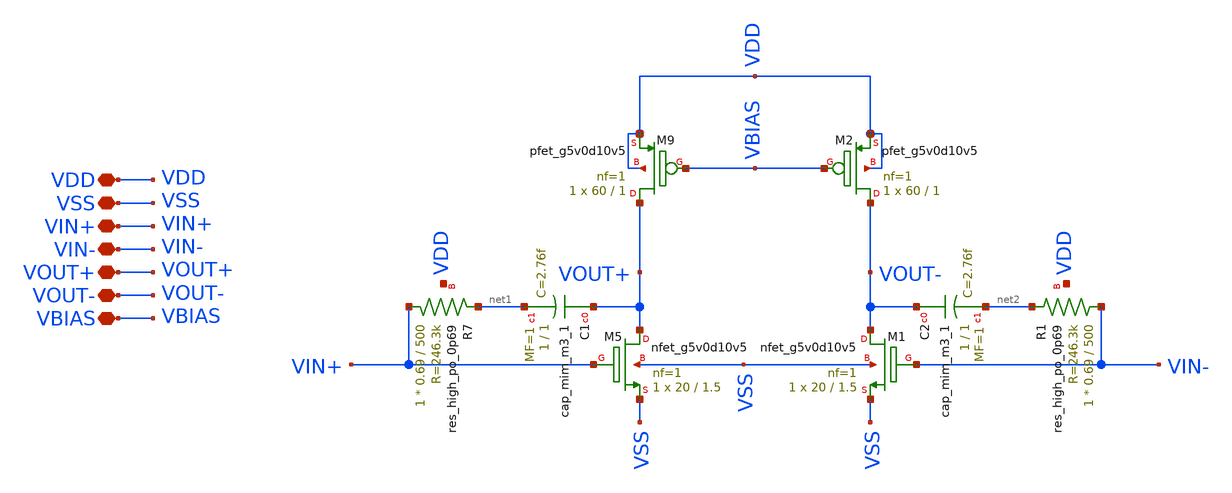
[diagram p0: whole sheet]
** sch_path: folded_cascode_amplifier/2_stage/second_stage.sch
**.subckt second_stage VDD VSS VIN+ VIN- VOUT+ VOUT- VBIAS
*.iopin VDD
*.iopin VSS
*.iopin VIN+
*.iopin VIN-
*.iopin VOUT+
*.iopin VOUT-
*.iopin VBIAS
XM5 VOUT+ VIN+ VSS VSS sky130_fd_pr__nfet_g5v0d10v5 L=1.5 W=20 nf=1 ad='int((1 + 1)/2) * 20 / 1 * 0.29'
+ as='int((1 + 2)/2) * 20 / 1 * 0.29' pd='2*int((1 + 1)/2) * (20 / 1 + 0.29)' ps='2*int((1 + 2)/2) * (20 / 1 + 0.29)'
+ nrd='0.29 / 20 ' nrs='0.29 / 20 ' sa=0 sb=0 sd=0 mult=1 m=1
XM1 VOUT- VIN- VSS VSS sky130_fd_pr__nfet_g5v0d10v5 L=1.5 W=20 nf=1 ad='int((1 + 1)/2) * 20 / 1 * 0.29'
+ as='int((1 + 2)/2) * 20 / 1 * 0.29' pd='2*int((1 + 1)/2) * (20 / 1 + 0.29)' ps='2*int((1 + 2)/2) * (20 / 1 + 0.29)'
+ nrd='0.29 / 20 ' nrs='0.29 / 20 ' sa=0 sb=0 sd=0 mult=1 m=1
XM9 VOUT+ VBIAS VDD VDD sky130_fd_pr__pfet_g5v0d10v5 L=1 W=60 nf=1 ad='int((1 + 1)/2) * 60 / 1 * 0.29'
+ as='int((1 + 2)/2) * 60 / 1 * 0.29' pd='2*int((1 + 1)/2) * (60 / 1 + 0.29)' ps='2*int((1 + 2)/2) * (60 / 1 + 0.29)'
+ nrd='0.29 / 60 ' nrs='0.29 / 60 ' sa=0 sb=0 sd=0 mult=1 m=1
XM2 VOUT- VBIAS VDD VDD sky130_fd_pr__pfet_g5v0d10v5 L=1 W=60 nf=1 ad='int((1 + 1)/2) * 60 / 1 * 0.29'
+ as='int((1 + 2)/2) * 60 / 1 * 0.29' pd='2*int((1 + 1)/2) * (60 / 1 + 0.29)' ps='2*int((1 + 2)/2) * (60 / 1 + 0.29)'
+ nrd='0.29 / 60 ' nrs='0.29 / 60 ' sa=0 sb=0 sd=0 mult=1 m=1
XR7 VIN+ net1 VDD sky130_fd_pr__res_high_po_0p69 L=500 mult=1 m=1
XC1 VOUT+ net1 sky130_fd_pr__cap_mim_m3_1 W=1 L=1 MF=1 m=1
XC2 VOUT- net2 sky130_fd_pr__cap_mim_m3_1 W=1 L=1 MF=1 m=1
XR1 VIN- net2 VDD sky130_fd_pr__res_high_po_0p69 L=500 mult=1 m=1
**.ends
.end
